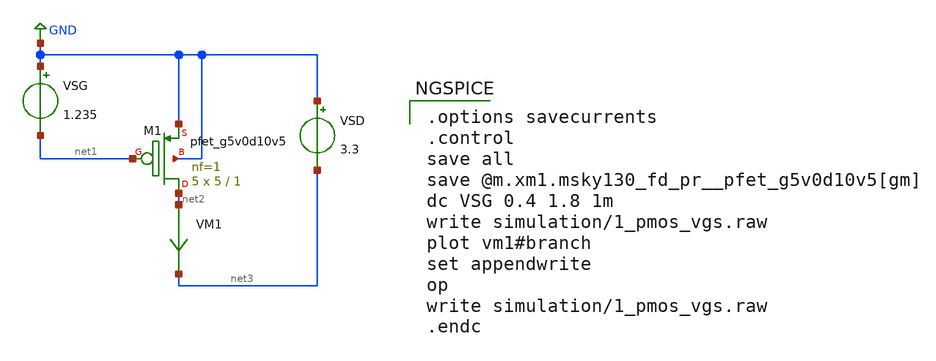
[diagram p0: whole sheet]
** sch_path: xschem/1_pmos_vgs.sch
**.subckt 1_pmos_vgs
VSG GND net1 1.235
VSD GND net3 3.3
VM1 net2 net3 0
.save i(vm1)
XM1 net2 net1 GND GND sky130_fd_pr__pfet_g5v0d10v5 L=1 W=5 nf=1 ad='int((nf+1)/2) * W/nf * 0.29' as='int((nf+2)/2) * W/nf * 0.29'
+ pd='2*int((nf+1)/2) * (W/nf + 0.29)' ps='2*int((nf+2)/2) * (W/nf + 0.29)' nrd='0.29 / W' nrs='0.29 / W'
+ sa=0 sb=0 sd=0 mult=5 m=5
**** begin user architecture code

.options savecurrents
.control
save all
save @m.xm1.msky130_fd_pr__pfet_g5v0d10v5[gm]
dc VSG 0.4 1.8 1m
write simulation/1_pmos_vgs.raw
plot vm1#branch
set appendwrite
op
write simulation/1_pmos_vgs.raw
.endc



** opencircuitdesign pdks install
.lib $::SKYWATER_MODELS/sky130.lib.spice tt


**** end user architecture code
**.ends
.GLOBAL GND
.end
